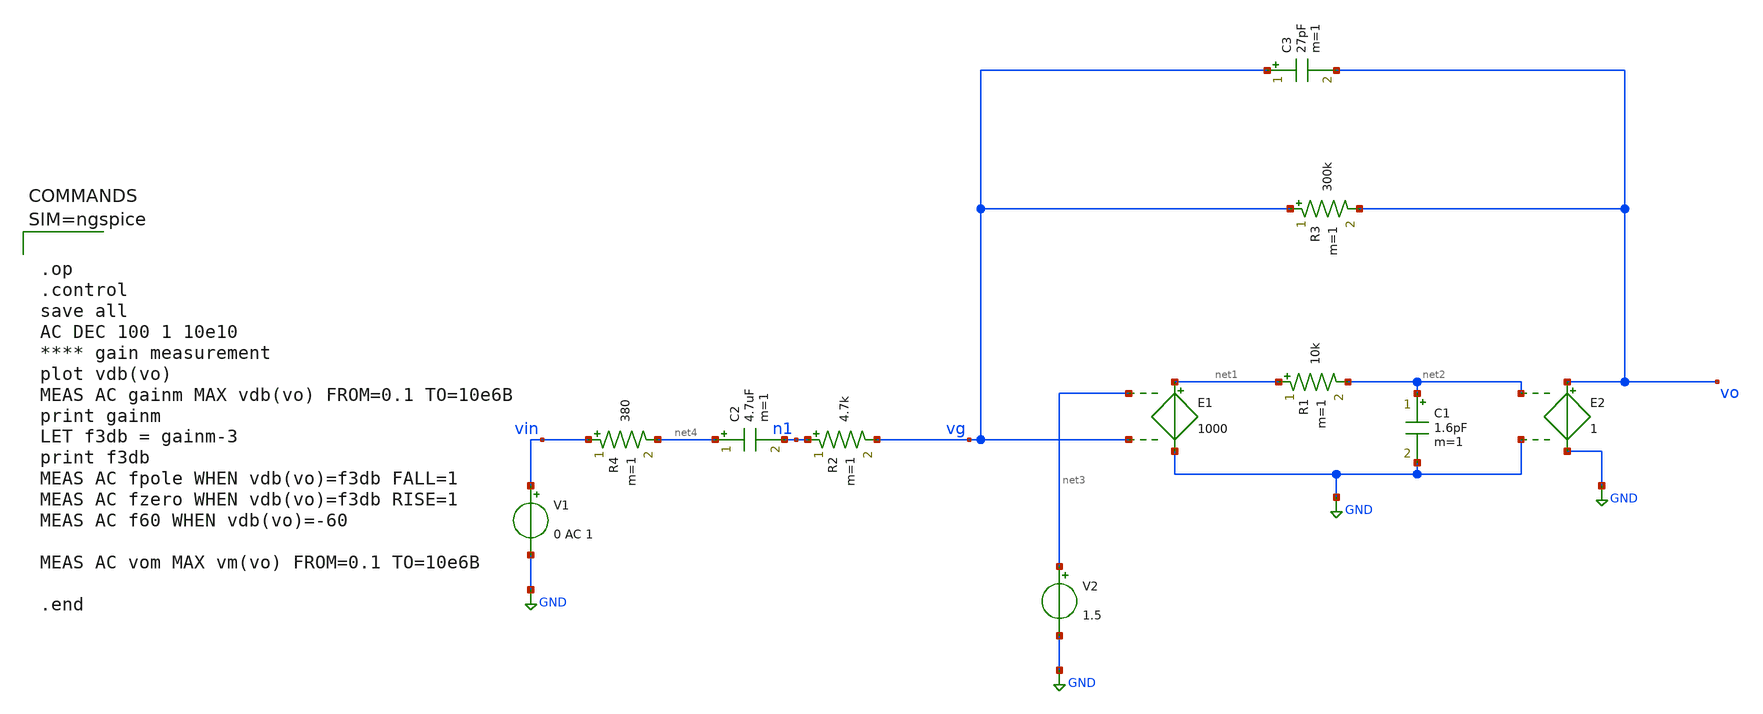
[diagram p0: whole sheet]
** sch_path: Work/xschem/2_vcvs.sch
**.subckt 2_vcvs
E1 net1 GND net3 vg 1000
E2 vo GND net2 GND 1
R1 net1 net2 10k m=1
C1 net2 GND 1.6pF m=1
V1 vin GND 0 AC 1
V2 net3 GND 1.5
R2 n1 vg 4.7k m=1
R3 vg vo 300k m=1
C2 net4 n1 4.7uF m=1
C3 vg vo 27pF m=1
R4 vin net4 380 m=1
**** begin user architecture code



.op
.control
save all
AC DEC 100 1 10e10
**** gain measurement
plot vdb(vo)
MEAS AC gainm MAX vdb(vo) FROM=0.1 TO=10e6B
print gainm
LET f3db = gainm-3
print f3db
MEAS AC fpole WHEN vdb(vo)=f3db FALL=1
MEAS AC fzero WHEN vdb(vo)=f3db RISE=1
MEAS AC f60 WHEN vdb(vo)=-60

MEAS AC vom MAX vm(vo) FROM=0.1 TO=10e6B

.end



**** end user architecture code
**.ends
.GLOBAL GND
.end
